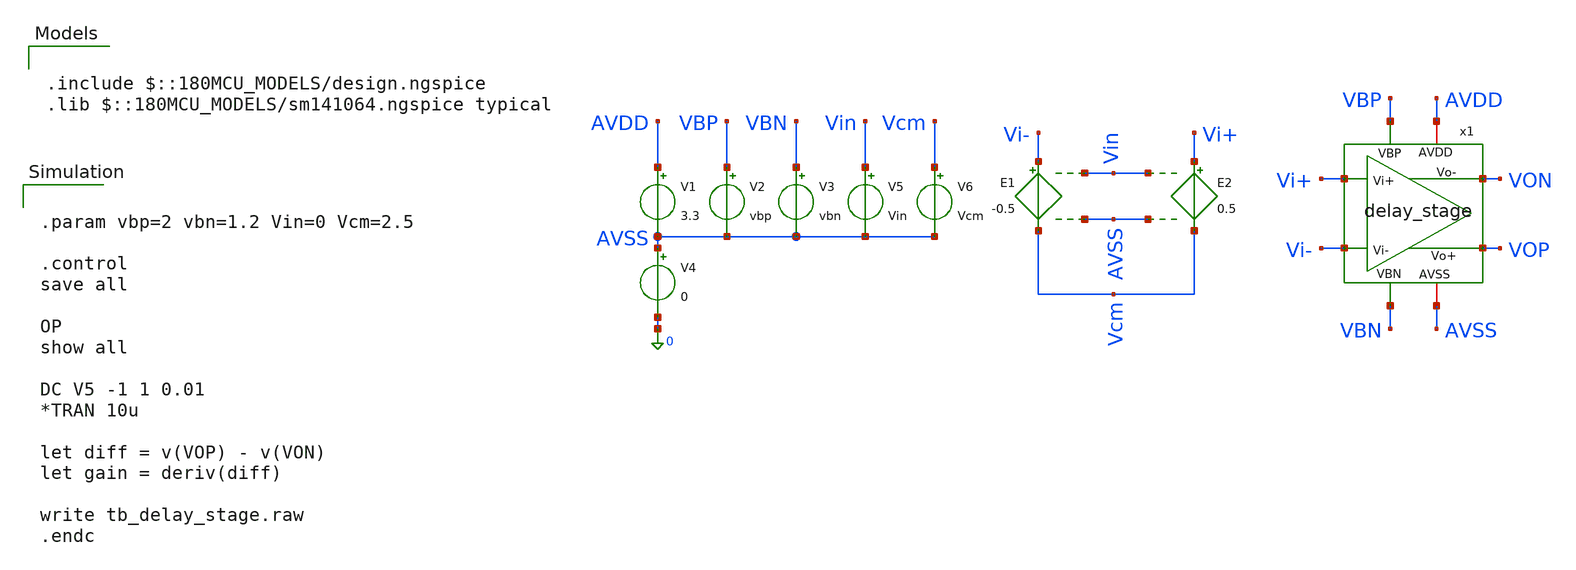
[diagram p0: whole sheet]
** sch_path: designs/libs/tb_analog/tb_delay_stage/tb_delay_stage.sch
**.subckt tb_delay_stage
x1 VOP AVDD Vi+ Vi- VON AVSS VBP VBN delay_stage
V1 AVDD AVSS 3.3
V2 VBP AVSS vbp
V3 VBN AVSS vbn
V4 AVSS 0 0
E1 Vi- Vcm Vin AVSS -0.5
E2 Vi+ Vcm Vin AVSS 0.5
V5 Vin AVSS Vin
V6 Vcm AVSS Vcm
**** begin user architecture code


.param vbp=2 vbn=1.2 Vin=0 Vcm=2.5

.control
save all

OP
show all

DC V5 -1 1 0.01
*TRAN 10u

let diff = v(VOP) - v(VON)
let gain = deriv(diff)

write tb_delay_stage.raw
.endc



.include $::180MCU_MODELS/design.ngspice
.lib $::180MCU_MODELS/sm141064.ngspice typical

**** end user architecture code
**.ends

* expanding   symbol:  libs/core_analog/delay_stage/delay_stage.sym # of pins=8
** sym_path: designs/libs/core_analog/delay_stage/delay_stage.sym
** sch_path: designs/libs/core_analog/delay_stage/delay_stage.sch
.subckt delay_stage Vo+ AVDD Vi+ Vi- Vo- AVSS VBP VBN
*.ipin Vi+
*.ipin Vi-
*.opin Vo+
*.opin Vo-
*.iopin AVDD
*.iopin AVSS
*.ipin VBP
*.ipin VBN
XM1 Vo- Vo- AVDD AVDD pfet_03v3 L=0.28u W=0.22u nf=1 ad='int((nf+1)/2) * W/nf * 0.18u' as='int((nf+2)/2) * W/nf * 0.18u'
+ pd='2*int((nf+1)/2) * (W/nf + 0.18u)' ps='2*int((nf+2)/2) * (W/nf + 0.18u)' nrd='0.18u / W' nrs='0.18u / W'
+ sa=0 sb=0 sd=0 m=1
XM2 Vo- VBP AVDD AVDD pfet_03v3 L=0.28u W=0.22u nf=1 ad='int((nf+1)/2) * W/nf * 0.18u' as='int((nf+2)/2) * W/nf * 0.18u'
+ pd='2*int((nf+1)/2) * (W/nf + 0.18u)' ps='2*int((nf+2)/2) * (W/nf + 0.18u)' nrd='0.18u / W' nrs='0.18u / W'
+ sa=0 sb=0 sd=0 m=1
XM3 Vo+ VBP AVDD AVDD pfet_03v3 L=0.28u W=0.22u nf=1 ad='int((nf+1)/2) * W/nf * 0.18u' as='int((nf+2)/2) * W/nf * 0.18u'
+ pd='2*int((nf+1)/2) * (W/nf + 0.18u)' ps='2*int((nf+2)/2) * (W/nf + 0.18u)' nrd='0.18u / W' nrs='0.18u / W'
+ sa=0 sb=0 sd=0 m=1
XM4 Vo+ Vo+ AVDD AVDD pfet_03v3 L=0.28u W=0.22u nf=1 ad='int((nf+1)/2) * W/nf * 0.18u' as='int((nf+2)/2) * W/nf * 0.18u'
+ pd='2*int((nf+1)/2) * (W/nf + 0.18u)' ps='2*int((nf+2)/2) * (W/nf + 0.18u)' nrd='0.18u / W' nrs='0.18u / W'
+ sa=0 sb=0 sd=0 m=1
XM5 Vo- Vi+ net1 AVSS nfet_03v3 L=0.28u W=0.22u nf=1 ad='int((nf+1)/2) * W/nf * 0.18u' as='int((nf+2)/2) * W/nf * 0.18u'
+ pd='2*int((nf+1)/2) * (W/nf + 0.18u)' ps='2*int((nf+2)/2) * (W/nf + 0.18u)' nrd='0.18u / W' nrs='0.18u / W'
+ sa=0 sb=0 sd=0 m=1
XM6 Vo+ Vi- net1 AVSS nfet_03v3 L=0.28u W=0.22u nf=1 ad='int((nf+1)/2) * W/nf * 0.18u' as='int((nf+2)/2) * W/nf * 0.18u'
+ pd='2*int((nf+1)/2) * (W/nf + 0.18u)' ps='2*int((nf+2)/2) * (W/nf + 0.18u)' nrd='0.18u / W' nrs='0.18u / W'
+ sa=0 sb=0 sd=0 m=1
XM7 net1 VBN AVSS AVSS nfet_03v3 L=0.28u W=0.22u nf=1 ad='int((nf+1)/2) * W/nf * 0.18u' as='int((nf+2)/2) * W/nf * 0.18u'
+ pd='2*int((nf+1)/2) * (W/nf + 0.18u)' ps='2*int((nf+2)/2) * (W/nf + 0.18u)' nrd='0.18u / W' nrs='0.18u / W'
+ sa=0 sb=0 sd=0 m=1
.ends

.end
